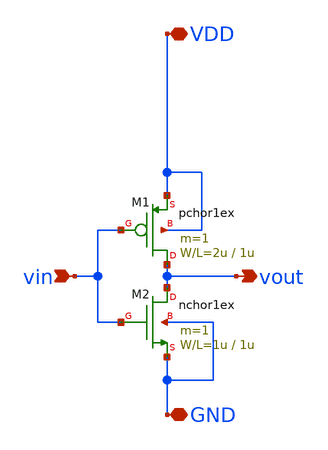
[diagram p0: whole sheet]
** sch_path: member_project/kensukeyama/koji/ishitra2.sch
**.subckt ishitra2 vout vin VDD GND
*.opin vout
*.ipin vin
*.iopin VDD
*.iopin GND
M1 vout vin VDD VDD pchor1ex L=1u W=2u m=1
M2 vout vin GND GND nchor1ex L=1u W=1u m=1
**.ends
.end
